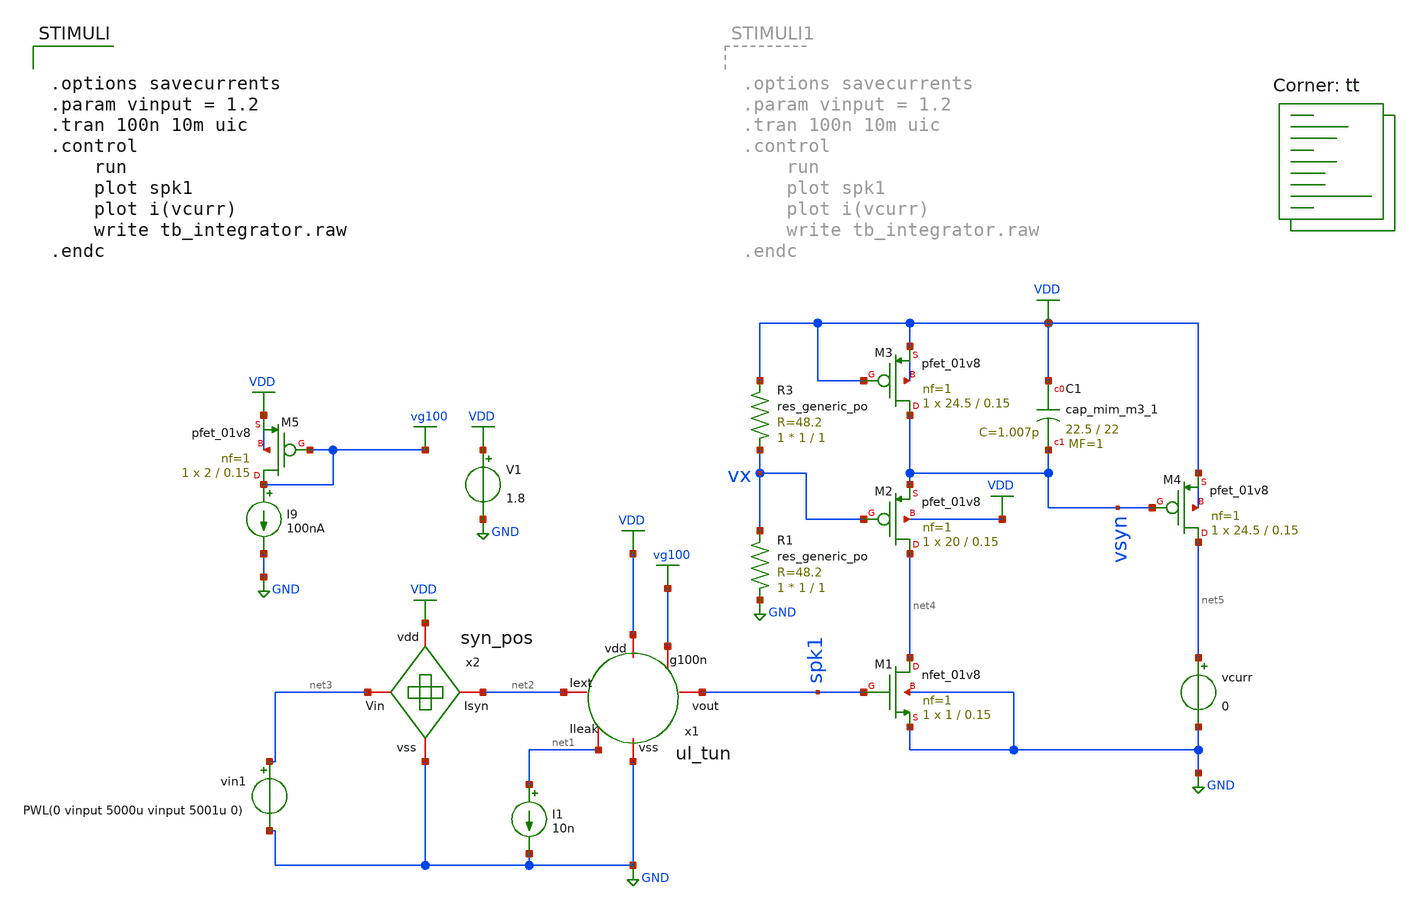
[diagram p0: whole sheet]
** sch_path: Neuron/ultralif/tb_integrator.sch
**.subckt tb_integrator
XM1 net4 spk1 GND GND sky130_fd_pr__nfet_01v8 L=0.15 W=1 nf=1 ad='int((nf+1)/2) * W/nf * 0.29' as='int((nf+2)/2) * W/nf * 0.29'
+ pd='2*int((nf+1)/2) * (W/nf + 0.29)' ps='2*int((nf+2)/2) * (W/nf + 0.29)' nrd='0.29 / W' nrs='0.29 / W'
+ sa=0 sb=0 sd=0 mult=1 m=1
XM2 net4 vx vsyn VDD sky130_fd_pr__pfet_01v8 L=0.15 W=20 nf=1 ad='int((nf+1)/2) * W/nf * 0.29' as='int((nf+2)/2) * W/nf * 0.29'
+ pd='2*int((nf+1)/2) * (W/nf + 0.29)' ps='2*int((nf+2)/2) * (W/nf + 0.29)' nrd='0.29 / W' nrs='0.29 / W'
+ sa=0 sb=0 sd=0 mult=1 m=1
XM3 vsyn VDD VDD VDD sky130_fd_pr__pfet_01v8 L=0.15 W=24.5 nf=1 ad='int((nf+1)/2) * W/nf * 0.29' as='int((nf+2)/2) * W/nf * 0.29'
+ pd='2*int((nf+1)/2) * (W/nf + 0.29)' ps='2*int((nf+2)/2) * (W/nf + 0.29)' nrd='0.29 / W' nrs='0.29 / W'
+ sa=0 sb=0 sd=0 mult=1 m=1
XM4 net5 vsyn VDD VDD sky130_fd_pr__pfet_01v8 L=0.15 W=24.5 nf=1 ad='int((nf+1)/2) * W/nf * 0.29' as='int((nf+2)/2) * W/nf * 0.29'
+ pd='2*int((nf+1)/2) * (W/nf + 0.29)' ps='2*int((nf+2)/2) * (W/nf + 0.29)' nrd='0.29 / W' nrs='0.29 / W'
+ sa=0 sb=0 sd=0 mult=1 m=1
XC1 VDD vsyn sky130_fd_pr__cap_mim_m3_1 W=22.5 L=22 MF=1 m=1
V1 VDD GND 1.8
I1 net1 GND 10n
x1 net2 VDD vg100 spk1 net1 GND ul_tun
I9 vg100 GND 100nA
XM5 vg100 vg100 VDD VDD sky130_fd_pr__pfet_01v8 L=0.15 W=2 nf=1 ad='int((nf+1)/2) * W/nf * 0.29' as='int((nf+2)/2) * W/nf * 0.29'
+ pd='2*int((nf+1)/2) * (W/nf + 0.29)' ps='2*int((nf+2)/2) * (W/nf + 0.29)' nrd='0.29 / W' nrs='0.29 / W'
+ sa=0 sb=0 sd=0 mult=1 m=1
vcurr net5 GND 0
vin1 net3 GND PWL(0 vinput 5000u vinput 5001u 0)
x2 VDD net3 net2 GND syn_pos
XR3 vx VDD sky130_fd_pr__res_generic_po W=1 L=1 m=1
XR1 GND vx sky130_fd_pr__res_generic_po W=1 L=1 m=1
**** begin user architecture code
.lib $::SKYWATER_MODELS/sky130.lib.spice tt
**** end user architecture code
**.ends

* expanding   symbol:  ul_tun.sym # of pins=6
** sym_path: Neuron/ultralif/ul_tun.sym
** sch_path: Neuron/ultralif/ul_tun.sch
.subckt ul_tun Iext vdd g100n vout Ileak vss
*.iopin Iext
*.iopin vout
*.iopin vss
*.iopin Ileak
*.iopin vdd
*.iopin g100n
XM1 Ileak Ileak net1 vdd sky130_fd_pr__pfet_01v8 L=10 W=1 nf=1 ad='int((nf+1)/2) * W/nf * 0.29' as='int((nf+2)/2) * W/nf * 0.29'
+ pd='2*int((nf+1)/2) * (W/nf + 0.29)' ps='2*int((nf+2)/2) * (W/nf + 0.29)' nrd='0.29 / W' nrs='0.29 / W'
+ sa=0 sb=0 sd=0 mult=1 m=1
XM2 Ileak net2 net1 vdd sky130_fd_pr__pfet_01v8 L=0.15 W=1.5 nf=1 ad='int((nf+1)/2) * W/nf * 0.29' as='int((nf+2)/2) * W/nf * 0.29'
+ pd='2*int((nf+1)/2) * (W/nf + 0.29)' ps='2*int((nf+2)/2) * (W/nf + 0.29)' nrd='0.29 / W' nrs='0.29 / W'
+ sa=0 sb=0 sd=0 mult=1 m=1
XM3 net2 net2 net1 vdd sky130_fd_pr__pfet_01v8 L=0.15 W=15 nf=1 ad='int((nf+1)/2) * W/nf * 0.29' as='int((nf+2)/2) * W/nf * 0.29'
+ pd='2*int((nf+1)/2) * (W/nf + 0.29)' ps='2*int((nf+2)/2) * (W/nf + 0.29)' nrd='0.29 / W' nrs='0.29 / W'
+ sa=0 sb=0 sd=0 mult=1 m=1
XM4 net2 Ileak vss vss sky130_fd_pr__nfet_01v8 L=4 W=1 nf=1 ad='int((1 + 1)/2) * 1 / 1 * 0.29' as='int((1 + 2)/2) * 1 / 1 * 0.29'
+ pd='2*int((1 + 1)/2) * (1 / 1 + 0.29)' ps='2*int((1 + 2)/2) * (1 / 1 + 0.29)' nrd='0.29 / 1 ' nrs='0.29 / 1 '
+ sa=0 sb=0 sd=0 mult=1 m=1
C1 net1 vss 1p m=1
XM5 vout_n Ileak vss vss sky130_fd_pr__nfet_01v8 L=0.15 W=1 nf=1 ad='int((1 + 1)/2) * 1 / 1 * 0.29' as='int((1 + 2)/2) * 1 / 1 * 0.29'
+ pd='2*int((1 + 1)/2) * (1 / 1 + 0.29)' ps='2*int((1 + 2)/2) * (1 / 1 + 0.29)' nrd='0.29 / 1 ' nrs='0.29 / 1 '
+ sa=0 sb=0 sd=0 mult=1 m=1
XM6 vout_n g100n vdd vdd sky130_fd_pr__pfet_01v8 L=0.15 W=2 nf=1 ad='int((nf+1)/2) * W/nf * 0.29' as='int((nf+2)/2) * W/nf * 0.29'
+ pd='2*int((nf+1)/2) * (W/nf + 0.29)' ps='2*int((nf+2)/2) * (W/nf + 0.29)' nrd='0.29 / W' nrs='0.29 / W'
+ sa=0 sb=0 sd=0 mult=1 m=1
XM7 vout vout_n vss vss sky130_fd_pr__nfet_01v8 L=0.15 W=1 nf=1 ad='int((1 + 1)/2) * 1 / 1 * 0.29' as='int((1 + 2)/2) * 1 / 1 * 0.29'
+ pd='2*int((1 + 1)/2) * (1 / 1 + 0.29)' ps='2*int((1 + 2)/2) * (1 / 1 + 0.29)' nrd='0.29 / 1 ' nrs='0.29 / 1 '
+ sa=0 sb=0 sd=0 mult=1 m=1
XM8 vout vout_n vdd vdd sky130_fd_pr__pfet_01v8 L=0.15 W=2 nf=1 ad='int((nf+1)/2) * W/nf * 0.29' as='int((nf+2)/2) * W/nf * 0.29'
+ pd='2*int((nf+1)/2) * (W/nf + 0.29)' ps='2*int((nf+2)/2) * (W/nf + 0.29)' nrd='0.29 / W' nrs='0.29 / W'
+ sa=0 sb=0 sd=0 mult=1 m=1
vext Iext net1 0
**** begin user architecture code


.save i(vext)


**** end user architecture code
.ends


* expanding   symbol:  syn_pos.sym # of pins=4
** sym_path: Neuron/ultralif/syn_pos.sym
** sch_path: Neuron/ultralif/syn_pos.sch
.subckt syn_pos vdd Vin Isyn vss
*.iopin Vin
*.iopin vdd
*.iopin vss
*.iopin Isyn
XM9 Isyn vx vdd vdd sky130_fd_pr__pfet_01v8 L=1.1 W=0.5 nf=1 ad='int((nf+1)/2) * W/nf * 0.29' as='int((nf+2)/2) * W/nf * 0.29'
+ pd='2*int((nf+1)/2) * (W/nf + 0.29)' ps='2*int((nf+2)/2) * (W/nf + 0.29)' nrd='0.29 / W' nrs='0.29 / W'
+ sa=0 sb=0 sd=0 mult=1 m=1
XM10 vx vx vdd vdd sky130_fd_pr__pfet_01v8 L=0.15 W=0.5 nf=1 ad='int((nf+1)/2) * W/nf * 0.29' as='int((nf+2)/2) * W/nf * 0.29'
+ pd='2*int((nf+1)/2) * (W/nf + 0.29)' ps='2*int((nf+2)/2) * (W/nf + 0.29)' nrd='0.29 / W' nrs='0.29 / W'
+ sa=0 sb=0 sd=0 mult=5 m=5
XM12 vx Vin vss vss sky130_fd_pr__nfet_01v8 L=1 W=0.4 nf=1 ad='int((1 + 1)/2) * 0.4 / 1 * 0.29' as='int((1 + 2)/2) * 0.4 / 1 * 0.29'
+ pd='2*int((1 + 1)/2) * (0.4 / 1 + 0.29)' ps='2*int((1 + 2)/2) * (0.4 / 1 + 0.29)' nrd='0.29 / 0.4 ' nrs='0.29 / 0.4 '
+ sa=0 sb=0 sd=0 mult=1 m=1
XM1 Isyn net1 vdd vdd sky130_fd_pr__pfet_01v8 L=1 W=0.5 nf=1 ad='int((nf+1)/2) * W/nf * 0.29' as='int((nf+2)/2) * W/nf * 0.29'
+ pd='2*int((nf+1)/2) * (W/nf + 0.29)' ps='2*int((nf+2)/2) * (W/nf + 0.29)' nrd='0.29 / W' nrs='0.29 / W'
+ sa=0 sb=0 sd=0 mult=1 m=1
XR1 net1 vdd sky130_fd_pr__res_generic_po W=1.15 L=1 m=1
XR2 vss net1 sky130_fd_pr__res_generic_po W=1 L=1 m=1
.ends

.GLOBAL GND
.GLOBAL VDD
.GLOBAL vg100
**** begin user architecture code


.options savecurrents
.param vinput = 1.2
.tran 100n 10m uic
.control
	run
	plot spk1
	plot i(vcurr)
	write tb_integrator.raw
.endc


**** end user architecture code
.end
